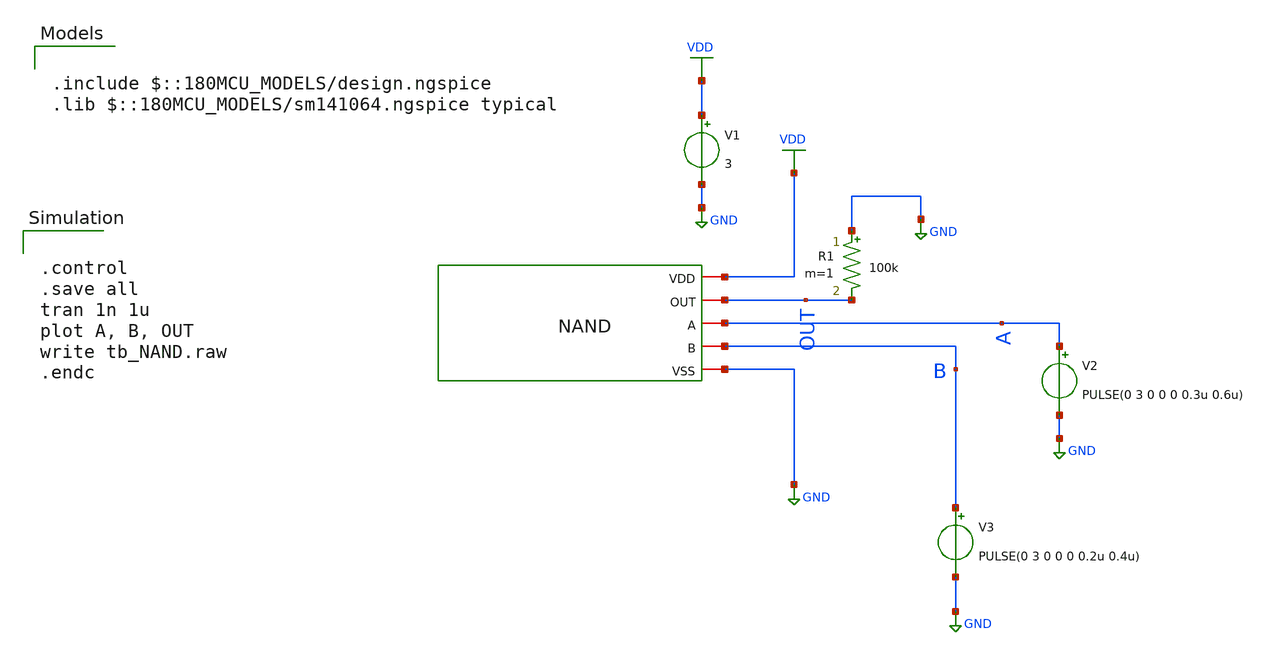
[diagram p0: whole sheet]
** sch_path: designs/libs/tb_analog/tb_nand/tb_NAND.sch
**.subckt tb_NAND
V1 VDD GND 3
V2 A GND PULSE(0 3 0 0 0 0.3u 0.6u)
V3 B GND PULSE(0 3 0 0 0 0.2u 0.4u)
R1 GND OUT 100k m=1
x1 VDD OUT A B GND NAND
**** begin user architecture code

.include $::180MCU_MODELS/design.ngspice
.lib $::180MCU_MODELS/sm141064.ngspice typical



.control
.save all
tran 1n 1u
plot A, B, OUT
write tb_NAND.raw
.endc


**** end user architecture code
**.ends
.GLOBAL GND
.GLOBAL VDD
.end
